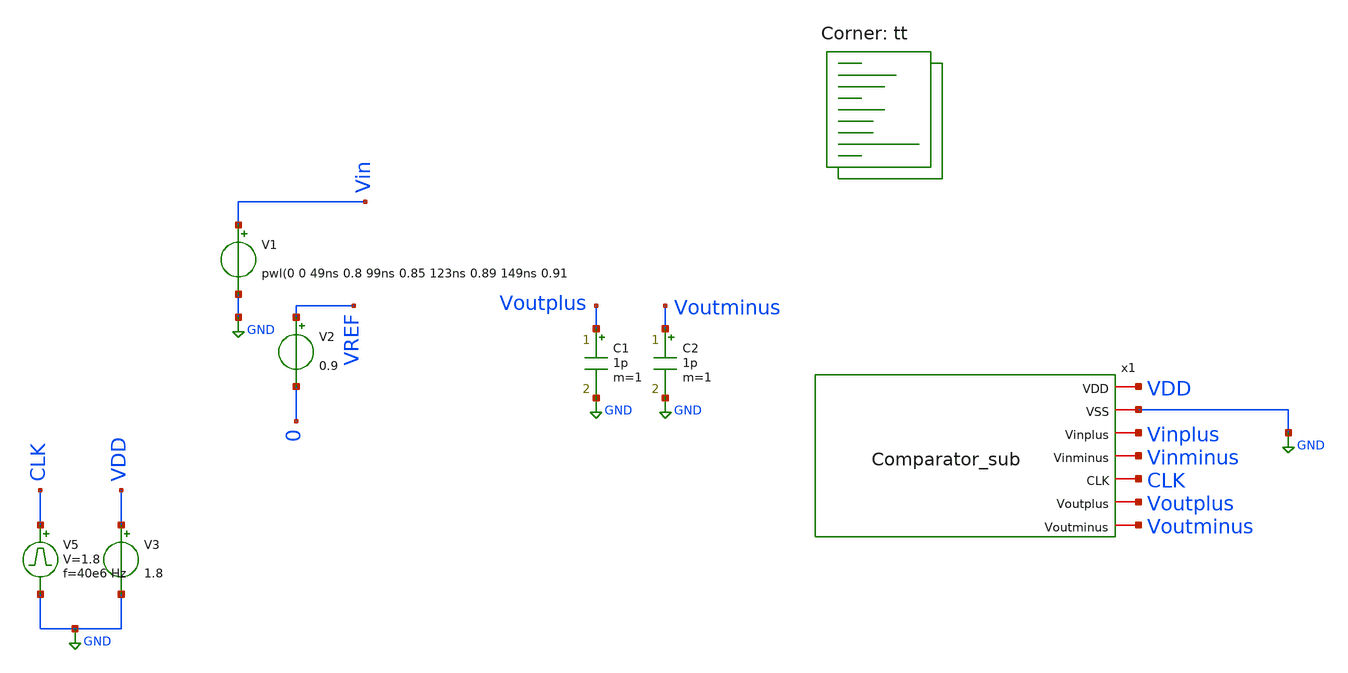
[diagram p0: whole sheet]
** sch_path: xschem/ComparatorTB.sch
**.subckt ComparatorTB
V2 VREF 0 0.9
V3 VDD GND 1.8
.save i(v3)
V1 Vin GND pwl(0 0 49ns 0.8 99ns 0.85 123ns 0.89 149ns 0.91
C1 Voutplus GND 1p m=1
C2 Voutminus GND 1p m=1
V5 CLK GND pulse 0 1.8 '0.495/ 40e6 ' '0.01/40e6 ' '0.01/40e6 ' '0.49/40e6 ' '1/40e6 '
x1 VDD GND Vinplus Vinminus CLK Voutplus Voutminus Comparator_sub
**** begin user architecture code


.include /home/jaxie963/caravel_pls_man_analog/caravel_user_project_analog/mag/comparator_hold/combination_test_WORKING.spice
.savecurrents
.control
save all

tran 1e-9 200e-9
plot Voutplus Voutminus
plot Vin CLK
plot Vin
print x1.Vds
let Vdif = Vin - Vref
let Voutdiff= Voutplus-Voutminus
plot Vdif Voutdiff
plot i(V3)
set filetype=binary
set appendwrite
write ComparatorTB.raw
.endc


.lib $::SKYWATER_MODELS/sky130.lib.spice tt
**** end user architecture code
**.ends

* expanding   symbol:  Comparator_sub.sym # of pins=7
** sym_path: xschem/Comparator_sub.sym
** sch_path: xschem/Comparator_sub.sch
.subckt Comparator_sub VDD VSS Vinplus Vinminus CLK Voutplus Voutminus
*.iopin VDD
*.iopin VSS
*.iopin Vinplus
*.iopin Vinminus
*.iopin CLK
*.iopin Voutplus
*.iopin Voutminus
XM11 Viominus Vinminus net1 VSS sky130_fd_pr__nfet_01v8 L=1 W=20 nf=1 ad='int((nf+1)/2) * W/nf * 0.29'
+ as='int((nf+2)/2) * W/nf * 0.29' pd='2*int((nf+1)/2) * (W/nf + 0.29)' ps='2*int((nf+2)/2) * (W/nf + 0.29)'
+ nrd='0.29 / W' nrs='0.29 / W' sa=0 sb=0 sd=0 mult=1 m=1
XM12 Vioplus Vinplus net1 VSS sky130_fd_pr__nfet_01v8 L=1 W=20 nf=1 ad='int((nf+1)/2) * W/nf * 0.29'
+ as='int((nf+2)/2) * W/nf * 0.29' pd='2*int((nf+1)/2) * (W/nf + 0.29)' ps='2*int((nf+2)/2) * (W/nf + 0.29)'
+ nrd='0.29 / W' nrs='0.29 / W' sa=0 sb=0 sd=0 mult=1 m=1
I0 net1 VSS 50u
XR1 Viominus VDD VSS sky130_fd_pr__res_xhigh_po W=1 L=10 mult=1 m=1
XR2 Vioplus VDD VSS sky130_fd_pr__res_xhigh_po W=1 L=10 mult=1 m=1
x1 VDD VSS CLK Voutplus Voutminus Vioplus Viominus combination_test_WORKING
.ends

.GLOBAL GND
.end
